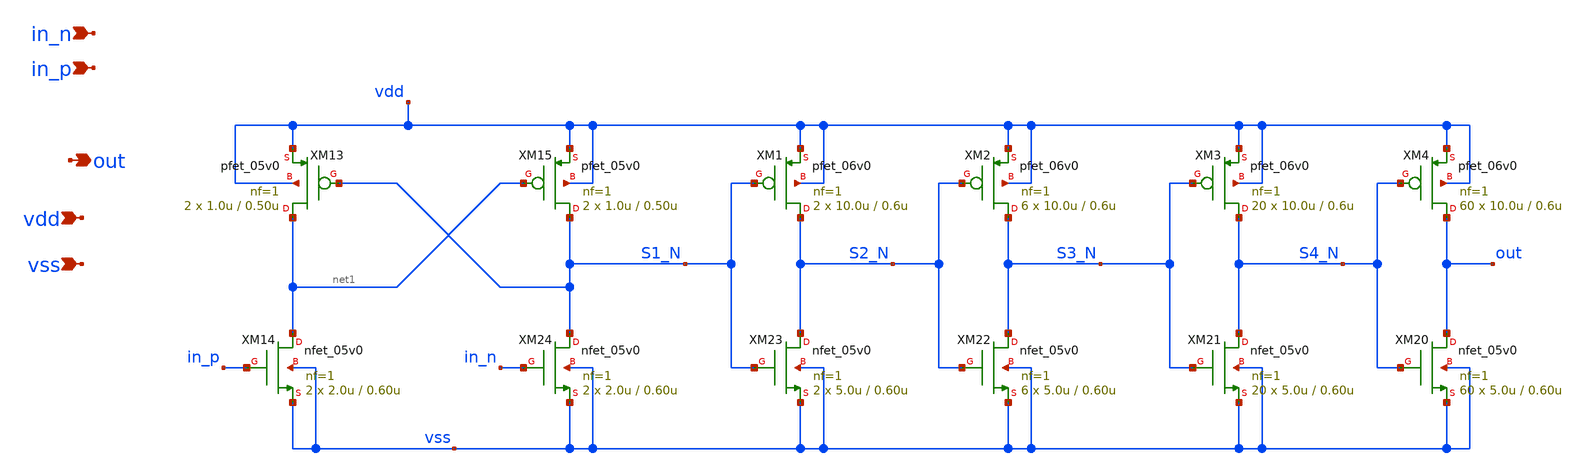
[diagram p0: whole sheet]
** sch_path: xschem/gate_drive_large.sch
**.subckt gate_drive_large in_n in_p vdd vss out
*.ipin in_n
*.ipin in_p
*.ipin vdd
*.ipin vss
*.opin out
XM13 net1 S1_N vdd vdd pfet_05v0 L=0.50u W=1.0u nf=1 ad='int((nf+1)/2) * W/nf * 0.18u' as='int((nf+2)/2) * W/nf * 0.18u'
+ pd='2*int((nf+1)/2) * (W/nf + 0.18u)' ps='2*int((nf+2)/2) * (W/nf + 0.18u)' nrd='0.18u / W' nrs='0.18u / W'
+ sa=0 sb=0 sd=0 m=2 par=2
XM14 net1 in_p vss vss nfet_05v0 L=0.60u W=2.0u nf=1 ad='int((nf+1)/2) * W/nf * 0.18u' as='int((nf+2)/2) * W/nf * 0.18u'
+ pd='2*int((nf+1)/2) * (W/nf + 0.18u)' ps='2*int((nf+2)/2) * (W/nf + 0.18u)' nrd='0.18u / W' nrs='0.18u / W'
+ sa=0 sb=0 sd=0 m=2
XM15 S1_N net1 vdd vdd pfet_05v0 L=0.50u W=1.0u nf=1 ad='int((nf+1)/2) * W/nf * 0.18u' as='int((nf+2)/2) * W/nf * 0.18u'
+ pd='2*int((nf+1)/2) * (W/nf + 0.18u)' ps='2*int((nf+2)/2) * (W/nf + 0.18u)' nrd='0.18u / W' nrs='0.18u / W'
+ sa=0 sb=0 sd=0 m=2 par=2
XM20 out S4_N vss vss nfet_05v0 L=0.60u W=5.0u nf=1 ad='int((nf+1)/2) * W/nf * 0.18u' as='int((nf+2)/2) * W/nf * 0.18u'
+ pd='2*int((nf+1)/2) * (W/nf + 0.18u)' ps='2*int((nf+2)/2) * (W/nf + 0.18u)' nrd='0.18u / W' nrs='0.18u / W'
+ sa=0 sb=0 sd=0 m=60
XM21 S4_N S3_N vss vss nfet_05v0 L=0.60u W=5.0u nf=1 ad='int((nf+1)/2) * W/nf * 0.18u' as='int((nf+2)/2) * W/nf * 0.18u'
+ pd='2*int((nf+1)/2) * (W/nf + 0.18u)' ps='2*int((nf+2)/2) * (W/nf + 0.18u)' nrd='0.18u / W' nrs='0.18u / W'
+ sa=0 sb=0 sd=0 m=20
XM22 S3_N S2_N vss vss nfet_05v0 L=0.60u W=5.0u nf=1 ad='int((nf+1)/2) * W/nf * 0.18u' as='int((nf+2)/2) * W/nf * 0.18u'
+ pd='2*int((nf+1)/2) * (W/nf + 0.18u)' ps='2*int((nf+2)/2) * (W/nf + 0.18u)' nrd='0.18u / W' nrs='0.18u / W'
+ sa=0 sb=0 sd=0 m=6
XM23 S2_N S1_N vss vss nfet_05v0 L=0.60u W=5.0u nf=1 ad='int((nf+1)/2) * W/nf * 0.18u' as='int((nf+2)/2) * W/nf * 0.18u'
+ pd='2*int((nf+1)/2) * (W/nf + 0.18u)' ps='2*int((nf+2)/2) * (W/nf + 0.18u)' nrd='0.18u / W' nrs='0.18u / W'
+ sa=0 sb=0 sd=0 m=2
XM24 S1_N in_n vss vss nfet_05v0 L=0.60u W=2.0u nf=1 ad='int((nf+1)/2) * W/nf * 0.18u' as='int((nf+2)/2) * W/nf * 0.18u'
+ pd='2*int((nf+1)/2) * (W/nf + 0.18u)' ps='2*int((nf+2)/2) * (W/nf + 0.18u)' nrd='0.18u / W' nrs='0.18u / W'
+ sa=0 sb=0 sd=0 m=2
XM1 S2_N S1_N vdd vdd pfet_06v0 L=0.6u W=10.0u nf=1 ad='int((nf+1)/2) * W/nf * 0.18u' as='int((nf+2)/2) * W/nf * 0.18u'
+ pd='2*int((nf+1)/2) * (W/nf + 0.18u)' ps='2*int((nf+2)/2) * (W/nf + 0.18u)' nrd='0.18u / W' nrs='0.18u / W'
+ sa=0 sb=0 sd=0 m=2
XM2 S3_N S2_N vdd vdd pfet_06v0 L=0.6u W=10.0u nf=1 ad='int((nf+1)/2) * W/nf * 0.18u' as='int((nf+2)/2) * W/nf * 0.18u'
+ pd='2*int((nf+1)/2) * (W/nf + 0.18u)' ps='2*int((nf+2)/2) * (W/nf + 0.18u)' nrd='0.18u / W' nrs='0.18u / W'
+ sa=0 sb=0 sd=0 m=6
XM3 S4_N S3_N vdd vdd pfet_06v0 L=0.6u W=10.0u nf=1 ad='int((nf+1)/2) * W/nf * 0.18u' as='int((nf+2)/2) * W/nf * 0.18u'
+ pd='2*int((nf+1)/2) * (W/nf + 0.18u)' ps='2*int((nf+2)/2) * (W/nf + 0.18u)' nrd='0.18u / W' nrs='0.18u / W'
+ sa=0 sb=0 sd=0 m=20
XM4 out S4_N vdd vdd pfet_06v0 L=0.6u W=10.0u nf=1 ad='int((nf+1)/2) * W/nf * 0.18u' as='int((nf+2)/2) * W/nf * 0.18u'
+ pd='2*int((nf+1)/2) * (W/nf + 0.18u)' ps='2*int((nf+2)/2) * (W/nf + 0.18u)' nrd='0.18u / W' nrs='0.18u / W'
+ sa=0 sb=0 sd=0 m=60
**.ends
.end
